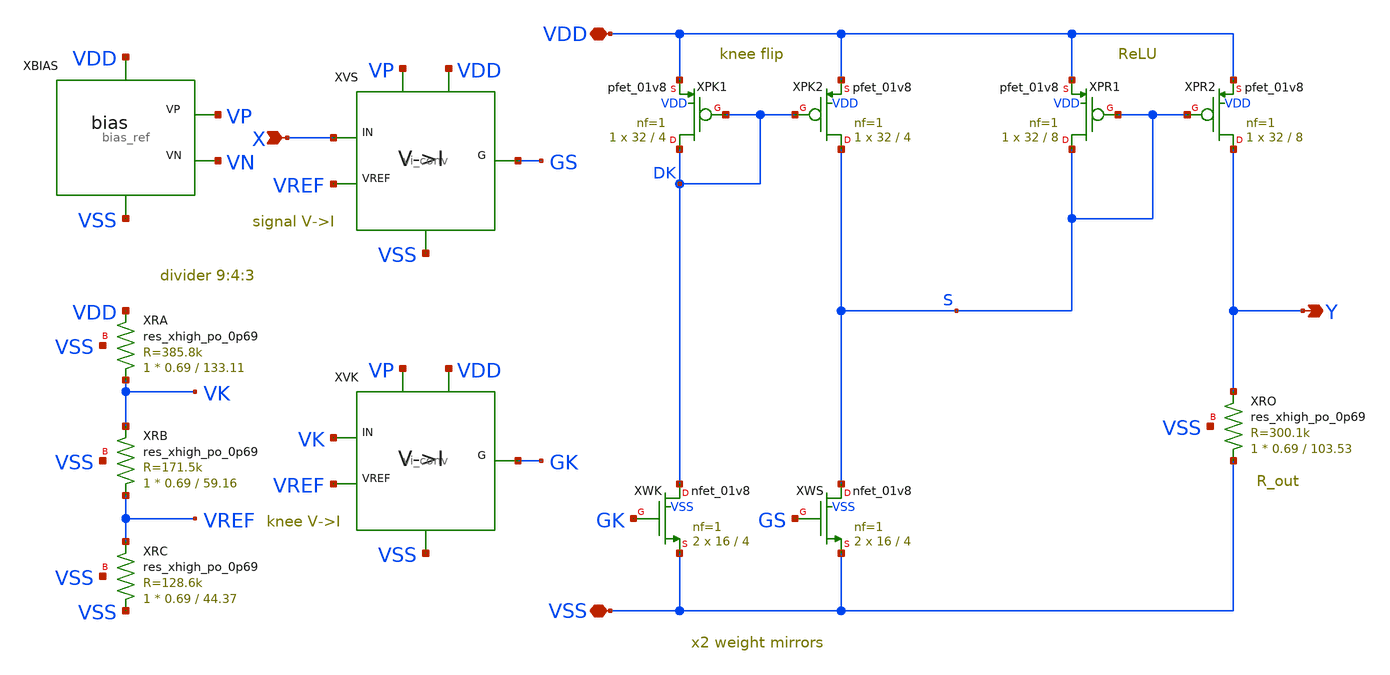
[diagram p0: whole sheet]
** sch_path: xschem/neuron_core.sch
**.subckt neuron_core X VDD VSS Y
*.ipin X
*.iopin VDD
*.iopin VSS
*.opin Y
XBIAS VDD VSS VP VN bias_ref
XXRA VK VDD VSS sky130_fd_pr__res_xhigh_po_0p69 L=133.11 mult=1 m=1
XXRB VREF VK VSS sky130_fd_pr__res_xhigh_po_0p69 L=59.16 mult=1 m=1
XXRC VSS VREF VSS sky130_fd_pr__res_xhigh_po_0p69 L=44.37 mult=1 m=1
XVS X VREF GS VP VDD VSS vi_conv
XVK VK VREF GK VP VDD VSS vi_conv
XXPK1 DK DK VDD VDD sky130_fd_pr__pfet_01v8 L=4 W=32 nf=1 ad='int((1 + 1)/2) * 32 / 1 * 0.29' as='int((1 + 2)/2) * 32 / 1 * 0.29'
+ pd='2*int((1 + 1)/2) * (32 / 1 + 0.29)' ps='2*int((1 + 2)/2) * (32 / 1 + 0.29)' nrd='0.29 / 32 ' nrs='0.29 / 32 '
+ sa=0 sb=0 sd=0 mult=1 m=1
XXPK2 S DK VDD VDD sky130_fd_pr__pfet_01v8 L=4 W=32 nf=1 ad='int((1 + 1)/2) * 32 / 1 * 0.29' as='int((1 + 2)/2) * 32 / 1 * 0.29'
+ pd='2*int((1 + 1)/2) * (32 / 1 + 0.29)' ps='2*int((1 + 2)/2) * (32 / 1 + 0.29)' nrd='0.29 / 32 ' nrs='0.29 / 32 '
+ sa=0 sb=0 sd=0 mult=1 m=1
XXWK DK GK VSS VSS sky130_fd_pr__nfet_01v8 L=4 W=16 nf=1 ad='int((nf+1)/2) * W/nf * 0.29' as='int((nf+2)/2) * W/nf * 0.29'
+ pd='2*int((nf+1)/2) * (W/nf + 0.29)' ps='2*int((nf+2)/2) * (W/nf + 0.29)' nrd='0.29 / W' nrs='0.29 / W'
+ sa=0 sb=0 sd=0 mult=2 m=2
XXWS S GS VSS VSS sky130_fd_pr__nfet_01v8 L=4 W=16 nf=1 ad='int((nf+1)/2) * W/nf * 0.29' as='int((nf+2)/2) * W/nf * 0.29'
+ pd='2*int((nf+1)/2) * (W/nf + 0.29)' ps='2*int((nf+2)/2) * (W/nf + 0.29)' nrd='0.29 / W' nrs='0.29 / W'
+ sa=0 sb=0 sd=0 mult=2 m=2
XXPR1 S S VDD VDD sky130_fd_pr__pfet_01v8 L=8 W=32 nf=1 ad='int((1 + 1)/2) * 32 / 1 * 0.29' as='int((1 + 2)/2) * 32 / 1 * 0.29'
+ pd='2*int((1 + 1)/2) * (32 / 1 + 0.29)' ps='2*int((1 + 2)/2) * (32 / 1 + 0.29)' nrd='0.29 / 32 ' nrs='0.29 / 32 '
+ sa=0 sb=0 sd=0 mult=1 m=1
XXPR2 Y S VDD VDD sky130_fd_pr__pfet_01v8 L=8 W=32 nf=1 ad='int((1 + 1)/2) * 32 / 1 * 0.29' as='int((1 + 2)/2) * 32 / 1 * 0.29'
+ pd='2*int((1 + 1)/2) * (32 / 1 + 0.29)' ps='2*int((1 + 2)/2) * (32 / 1 + 0.29)' nrd='0.29 / 32 ' nrs='0.29 / 32 '
+ sa=0 sb=0 sd=0 mult=1 m=1
XXRO VSS Y VSS sky130_fd_pr__res_xhigh_po_0p69 L=103.53 mult=1 m=1
**.ends

* expanding   symbol:  bias_ref.sym # of pins=4
** sym_path: xschem/bias_ref.sym
** sch_path: xschem/bias_ref.sch
.subckt bias_ref VDD VSS VP VN
*.opin VP
*.opin VN
*.iopin VDD
*.iopin VSS
XXM3 VN VP VDD VDD sky130_fd_pr__pfet_01v8 L=2 W=16 nf=1 ad='int((1 + 1)/2) * 16 / 1 * 0.29' as='int((1 + 2)/2) * 16 / 1 * 0.29'
+ pd='2*int((1 + 1)/2) * (16 / 1 + 0.29)' ps='2*int((1 + 2)/2) * (16 / 1 + 0.29)' nrd='0.29 / 16 ' nrs='0.29 / 16 '
+ sa=0 sb=0 sd=0 mult=1 m=1
XXM4 VP VP VDD VDD sky130_fd_pr__pfet_01v8 L=2 W=16 nf=1 ad='int((1 + 1)/2) * 16 / 1 * 0.29' as='int((1 + 2)/2) * 16 / 1 * 0.29'
+ pd='2*int((1 + 1)/2) * (16 / 1 + 0.29)' ps='2*int((1 + 2)/2) * (16 / 1 + 0.29)' nrd='0.29 / 16 ' nrs='0.29 / 16 '
+ sa=0 sb=0 sd=0 mult=1 m=1
XXM1 VN VN VSS VSS sky130_fd_pr__nfet_01v8 L=2 W=20 nf=1 ad='int((nf+1)/2) * W/nf * 0.29' as='int((nf+2)/2) * W/nf * 0.29'
+ pd='2*int((nf+1)/2) * (W/nf + 0.29)' ps='2*int((nf+2)/2) * (W/nf + 0.29)' nrd='0.29 / W' nrs='0.29 / W'
+ sa=0 sb=0 sd=0 mult=1 m=1
XXM2 VP VN net1 VSS sky130_fd_pr__nfet_01v8 L=2 W=20 nf=1 ad='int((nf+1)/2) * W/nf * 0.29' as='int((nf+2)/2) * W/nf * 0.29'
+ pd='2*int((nf+1)/2) * (W/nf + 0.29)' ps='2*int((nf+2)/2) * (W/nf + 0.29)' nrd='0.29 / W' nrs='0.29 / W'
+ sa=0 sb=0 sd=0 mult=4 m=4
XXR1 VSS net1 VSS sky130_fd_pr__res_xhigh_po_1p41 L=17 mult=1 m=1
XXMS1A net2 VSS VDD VDD sky130_fd_pr__pfet_01v8 L=40 W=0.42 nf=1 ad='int((1 + 1)/2) * 0.42 / 1 * 0.29'
+ as='int((1 + 2)/2) * 0.42 / 1 * 0.29' pd='2*int((1 + 1)/2) * (0.42 / 1 + 0.29)' ps='2*int((1 + 2)/2) * (0.42 / 1 + 0.29)'
+ nrd='0.29 / 0.42 ' nrs='0.29 / 0.42 ' sa=0 sb=0 sd=0 mult=1 m=1
XXMS1B ST VSS net2 VDD sky130_fd_pr__pfet_01v8 L=40 W=0.42 nf=1 ad='int((1 + 1)/2) * 0.42 / 1 * 0.29'
+ as='int((1 + 2)/2) * 0.42 / 1 * 0.29' pd='2*int((1 + 1)/2) * (0.42 / 1 + 0.29)' ps='2*int((1 + 2)/2) * (0.42 / 1 + 0.29)'
+ nrd='0.29 / 0.42 ' nrs='0.29 / 0.42 ' sa=0 sb=0 sd=0 mult=1 m=1
XXMS2 ST VN VSS VSS sky130_fd_pr__nfet_01v8 L=0.5 W=16 nf=1 ad='int((nf+1)/2) * W/nf * 0.29' as='int((nf+2)/2) * W/nf * 0.29'
+ pd='2*int((nf+1)/2) * (W/nf + 0.29)' ps='2*int((nf+2)/2) * (W/nf + 0.29)' nrd='0.29 / W' nrs='0.29 / W'
+ sa=0 sb=0 sd=0 mult=1 m=1
XXMS3 VDD ST VN VSS sky130_fd_pr__nfet_01v8 L=1 W=1 nf=1 ad='int((nf+1)/2) * W/nf * 0.29' as='int((nf+2)/2) * W/nf * 0.29'
+ pd='2*int((nf+1)/2) * (W/nf + 0.29)' ps='2*int((nf+2)/2) * (W/nf + 0.29)' nrd='0.29 / W' nrs='0.29 / W'
+ sa=0 sb=0 sd=0 mult=1 m=1
.ends


* expanding   symbol:  vi_conv.sym # of pins=6
** sym_path: xschem/vi_conv.sym
** sch_path: xschem/vi_conv.sch
.subckt vi_conv IN VREF G VP VDD VSS
*.ipin IN
*.ipin VREF
*.ipin VP
*.opin G
*.iopin VDD
*.iopin VSS
XXI0 X VP VDD VDD sky130_fd_pr__pfet_01v8 L=4 W=16 nf=1 ad='int((1 + 1)/2) * 16 / 1 * 0.29' as='int((1 + 2)/2) * 16 / 1 * 0.29'
+ pd='2*int((1 + 1)/2) * (16 / 1 + 0.29)' ps='2*int((1 + 2)/2) * (16 / 1 + 0.29)' nrd='0.29 / 16 ' nrs='0.29 / 16 '
+ sa=0 sb=0 sd=0 mult=1 m=1
XXMF X G VSS VSS sky130_fd_pr__nfet_01v8 L=4 W=16 nf=1 ad='int((nf+1)/2) * W/nf * 0.29' as='int((nf+2)/2) * W/nf * 0.29'
+ pd='2*int((nf+1)/2) * (W/nf + 0.29)' ps='2*int((nf+2)/2) * (W/nf + 0.29)' nrd='0.29 / W' nrs='0.29 / W'
+ sa=0 sb=0 sd=0 mult=1 m=1
XXR X IN VSS sky130_fd_pr__res_xhigh_po_0p69 L=103.53 mult=1 m=1
XXCC net1 X sky130_fd_pr__cap_mim_m3_1 W=20 L=20 MF=1 m=1
XXRZ net1 G VSS sky130_fd_pr__res_xhigh_po_0p69 L=25 mult=1 m=1
XA X VREF G VP VDD VSS ota5p
.ends


* expanding   symbol:  ota5p.sym # of pins=6
** sym_path: xschem/ota5p.sym
** sch_path: xschem/ota5p.sch
.subckt ota5p INP INN OUT VP VDD VSS
*.ipin INP
*.ipin INN
*.ipin VP
*.opin OUT
*.iopin VDD
*.iopin VSS
XXM1 D1 INP T T sky130_fd_pr__pfet_01v8 L=1 W=10 nf=1 ad='int((1 + 1)/2) * 10 / 1 * 0.29' as='int((1 + 2)/2) * 10 / 1 * 0.29'
+ pd='2*int((1 + 1)/2) * (10 / 1 + 0.29)' ps='2*int((1 + 2)/2) * (10 / 1 + 0.29)' nrd='0.29 / 10 ' nrs='0.29 / 10 '
+ sa=0 sb=0 sd=0 mult=1 m=1
XXM2 OUT INN T T sky130_fd_pr__pfet_01v8 L=1 W=10 nf=1 ad='int((1 + 1)/2) * 10 / 1 * 0.29' as='int((1 + 2)/2) * 10 / 1 * 0.29'
+ pd='2*int((1 + 1)/2) * (10 / 1 + 0.29)' ps='2*int((1 + 2)/2) * (10 / 1 + 0.29)' nrd='0.29 / 10 ' nrs='0.29 / 10 '
+ sa=0 sb=0 sd=0 mult=1 m=1
XXMT T VP VDD VDD sky130_fd_pr__pfet_01v8 L=2 W=16 nf=1 ad='int((1 + 1)/2) * 16 / 1 * 0.29' as='int((1 + 2)/2) * 16 / 1 * 0.29'
+ pd='2*int((1 + 1)/2) * (16 / 1 + 0.29)' ps='2*int((1 + 2)/2) * (16 / 1 + 0.29)' nrd='0.29 / 16 ' nrs='0.29 / 16 '
+ sa=0 sb=0 sd=0 mult=1 m=1
XXM3 D1 D1 VSS VSS sky130_fd_pr__nfet_01v8 L=2 W=2 nf=1 ad='int((nf+1)/2) * W/nf * 0.29' as='int((nf+2)/2) * W/nf * 0.29'
+ pd='2*int((nf+1)/2) * (W/nf + 0.29)' ps='2*int((nf+2)/2) * (W/nf + 0.29)' nrd='0.29 / W' nrs='0.29 / W'
+ sa=0 sb=0 sd=0 mult=1 m=1
XXM4 OUT D1 VSS VSS sky130_fd_pr__nfet_01v8 L=2 W=2 nf=1 ad='int((nf+1)/2) * W/nf * 0.29' as='int((nf+2)/2) * W/nf * 0.29'
+ pd='2*int((nf+1)/2) * (W/nf + 0.29)' ps='2*int((nf+2)/2) * (W/nf + 0.29)' nrd='0.29 / W' nrs='0.29 / W'
+ sa=0 sb=0 sd=0 mult=1 m=1
.ends

.end
